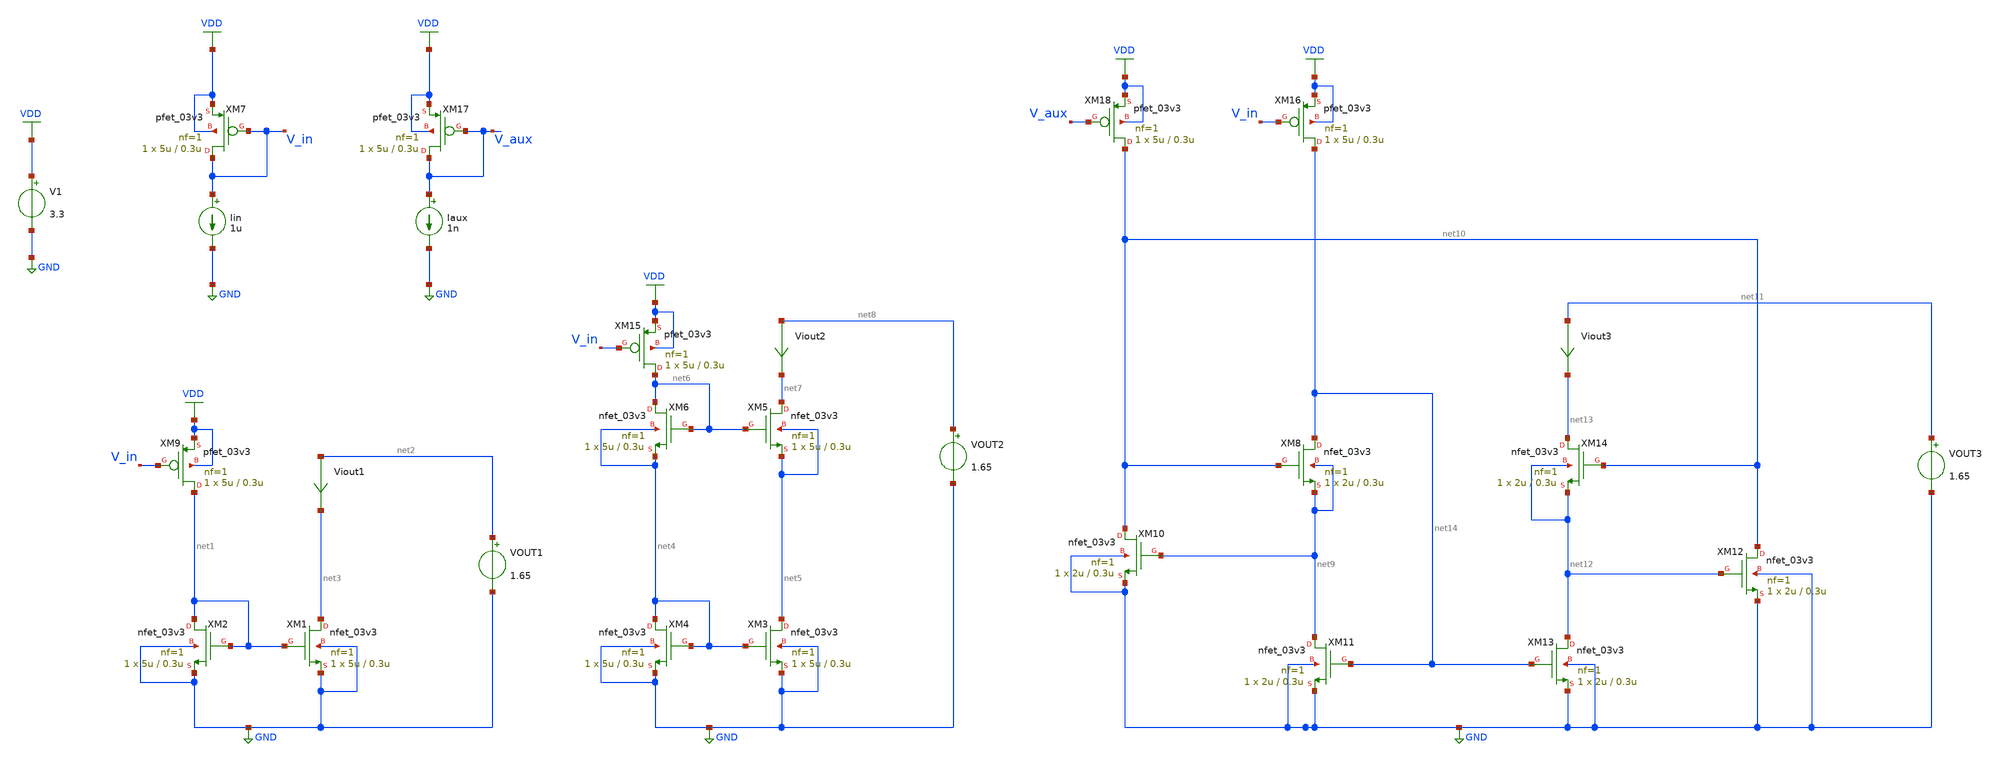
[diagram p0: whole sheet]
** sch_path: blocks/composite/regulated_cascoded_cmirror/xschem/current_mirror.sch
**.subckt current_mirror
XM1 net3 net1 GND GND nfet_03v3 L=0.3u W=5u nf=1 ad='int((nf+1)/2) * W/nf * 0.18u' as='int((nf+2)/2) * W/nf * 0.18u'
+ pd='2*int((nf+1)/2) * (W/nf + 0.18u)' ps='2*int((nf+2)/2) * (W/nf + 0.18u)' nrd='0.18u / W' nrs='0.18u / W'
+ sa=0 sb=0 sd=0 m=1
XM2 net1 net1 GND GND nfet_03v3 L=0.3u W=5u nf=1 ad='int((nf+1)/2) * W/nf * 0.18u' as='int((nf+2)/2) * W/nf * 0.18u'
+ pd='2*int((nf+1)/2) * (W/nf + 0.18u)' ps='2*int((nf+2)/2) * (W/nf + 0.18u)' nrd='0.18u / W' nrs='0.18u / W'
+ sa=0 sb=0 sd=0 m=1
VOUT1 net2 GND 1.65
.save i(vout1)
Viout1 net2 net3 0
.save i(viout1)
XM3 net5 net4 GND GND nfet_03v3 L=0.3u W=5u nf=1 ad='int((nf+1)/2) * W/nf * 0.18u' as='int((nf+2)/2) * W/nf * 0.18u'
+ pd='2*int((nf+1)/2) * (W/nf + 0.18u)' ps='2*int((nf+2)/2) * (W/nf + 0.18u)' nrd='0.18u / W' nrs='0.18u / W'
+ sa=0 sb=0 sd=0 m=1
XM4 net4 net4 GND GND nfet_03v3 L=0.3u W=5u nf=1 ad='int((nf+1)/2) * W/nf * 0.18u' as='int((nf+2)/2) * W/nf * 0.18u'
+ pd='2*int((nf+1)/2) * (W/nf + 0.18u)' ps='2*int((nf+2)/2) * (W/nf + 0.18u)' nrd='0.18u / W' nrs='0.18u / W'
+ sa=0 sb=0 sd=0 m=1
VOUT2 net8 GND 1.65
.save i(vout2)
Viout2 net8 net7 0
.save i(viout2)
XM5 net7 net6 net5 net5 nfet_03v3 L=0.3u W=5u nf=1 ad='int((nf+1)/2) * W/nf * 0.18u' as='int((nf+2)/2) * W/nf * 0.18u'
+ pd='2*int((nf+1)/2) * (W/nf + 0.18u)' ps='2*int((nf+2)/2) * (W/nf + 0.18u)' nrd='0.18u / W' nrs='0.18u / W'
+ sa=0 sb=0 sd=0 m=1
XM6 net6 net6 net4 net4 nfet_03v3 L=0.3u W=5u nf=1 ad='int((nf+1)/2) * W/nf * 0.18u' as='int((nf+2)/2) * W/nf * 0.18u'
+ pd='2*int((nf+1)/2) * (W/nf + 0.18u)' ps='2*int((nf+2)/2) * (W/nf + 0.18u)' nrd='0.18u / W' nrs='0.18u / W'
+ sa=0 sb=0 sd=0 m=1
VOUT3 net11 GND 1.65
.save i(vout3)
Viout3 net11 net13 0
.save i(viout3)
XM10 net10 net9 GND GND nfet_03v3 L=0.3u W=2u nf=1 ad='int((nf+1)/2) * W/nf * 0.18u' as='int((nf+2)/2) * W/nf * 0.18u'
+ pd='2*int((nf+1)/2) * (W/nf + 0.18u)' ps='2*int((nf+2)/2) * (W/nf + 0.18u)' nrd='0.18u / W' nrs='0.18u / W'
+ sa=0 sb=0 sd=0 m=1
XM8 net14 net10 net9 net9 nfet_03v3 L=0.3u W=2u nf=1 ad='int((nf+1)/2) * W/nf * 0.18u' as='int((nf+2)/2) * W/nf * 0.18u'
+ pd='2*int((nf+1)/2) * (W/nf + 0.18u)' ps='2*int((nf+2)/2) * (W/nf + 0.18u)' nrd='0.18u / W' nrs='0.18u / W'
+ sa=0 sb=0 sd=0 m=1
XM11 net9 net14 GND GND nfet_03v3 L=0.3u W=2u nf=1 ad='int((nf+1)/2) * W/nf * 0.18u' as='int((nf+2)/2) * W/nf * 0.18u'
+ pd='2*int((nf+1)/2) * (W/nf + 0.18u)' ps='2*int((nf+2)/2) * (W/nf + 0.18u)' nrd='0.18u / W' nrs='0.18u / W'
+ sa=0 sb=0 sd=0 m=1
XM12 net10 net12 GND GND nfet_03v3 L=0.3u W=2u nf=1 ad='int((nf+1)/2) * W/nf * 0.18u' as='int((nf+2)/2) * W/nf * 0.18u'
+ pd='2*int((nf+1)/2) * (W/nf + 0.18u)' ps='2*int((nf+2)/2) * (W/nf + 0.18u)' nrd='0.18u / W' nrs='0.18u / W'
+ sa=0 sb=0 sd=0 m=1
XM13 net12 net14 GND GND nfet_03v3 L=0.3u W=2u nf=1 ad='int((nf+1)/2) * W/nf * 0.18u' as='int((nf+2)/2) * W/nf * 0.18u'
+ pd='2*int((nf+1)/2) * (W/nf + 0.18u)' ps='2*int((nf+2)/2) * (W/nf + 0.18u)' nrd='0.18u / W' nrs='0.18u / W'
+ sa=0 sb=0 sd=0 m=1
XM14 net13 net10 net12 net12 nfet_03v3 L=0.3u W=2u nf=1 ad='int((nf+1)/2) * W/nf * 0.18u' as='int((nf+2)/2) * W/nf * 0.18u'
+ pd='2*int((nf+1)/2) * (W/nf + 0.18u)' ps='2*int((nf+2)/2) * (W/nf + 0.18u)' nrd='0.18u / W' nrs='0.18u / W'
+ sa=0 sb=0 sd=0 m=1
V1 VDD GND 3.3
XM7 V_in V_in VDD VDD pfet_03v3 L=0.3u W=5u nf=1 ad='int((nf+1)/2) * W/nf * 0.18u' as='int((nf+2)/2) * W/nf * 0.18u'
+ pd='2*int((nf+1)/2) * (W/nf + 0.18u)' ps='2*int((nf+2)/2) * (W/nf + 0.18u)' nrd='0.18u / W' nrs='0.18u / W'
+ sa=0 sb=0 sd=0 m=1
Iin V_in GND 1u
XM9 net1 V_in VDD VDD pfet_03v3 L=0.3u W=5u nf=1 ad='int((nf+1)/2) * W/nf * 0.18u' as='int((nf+2)/2) * W/nf * 0.18u'
+ pd='2*int((nf+1)/2) * (W/nf + 0.18u)' ps='2*int((nf+2)/2) * (W/nf + 0.18u)' nrd='0.18u / W' nrs='0.18u / W'
+ sa=0 sb=0 sd=0 m=1
XM15 net6 V_in VDD VDD pfet_03v3 L=0.3u W=5u nf=1 ad='int((nf+1)/2) * W/nf * 0.18u' as='int((nf+2)/2) * W/nf * 0.18u'
+ pd='2*int((nf+1)/2) * (W/nf + 0.18u)' ps='2*int((nf+2)/2) * (W/nf + 0.18u)' nrd='0.18u / W' nrs='0.18u / W'
+ sa=0 sb=0 sd=0 m=1
XM16 net14 V_in VDD VDD pfet_03v3 L=0.3u W=5u nf=1 ad='int((nf+1)/2) * W/nf * 0.18u' as='int((nf+2)/2) * W/nf * 0.18u'
+ pd='2*int((nf+1)/2) * (W/nf + 0.18u)' ps='2*int((nf+2)/2) * (W/nf + 0.18u)' nrd='0.18u / W' nrs='0.18u / W'
+ sa=0 sb=0 sd=0 m=1
XM17 V_aux V_aux VDD VDD pfet_03v3 L=0.3u W=5u nf=1 ad='int((nf+1)/2) * W/nf * 0.18u' as='int((nf+2)/2) * W/nf * 0.18u'
+ pd='2*int((nf+1)/2) * (W/nf + 0.18u)' ps='2*int((nf+2)/2) * (W/nf + 0.18u)' nrd='0.18u / W' nrs='0.18u / W'
+ sa=0 sb=0 sd=0 m=1
Iaux V_aux GND 1n
XM18 net10 V_aux VDD VDD pfet_03v3 L=0.3u W=5u nf=1 ad='int((nf+1)/2) * W/nf * 0.18u' as='int((nf+2)/2) * W/nf * 0.18u'
+ pd='2*int((nf+1)/2) * (W/nf + 0.18u)' ps='2*int((nf+2)/2) * (W/nf + 0.18u)' nrd='0.18u / W' nrs='0.18u / W'
+ sa=0 sb=0 sd=0 m=1
**** begin user architecture code



.option savecurrent
.control
save all

** Plot Vanilla Current Mirror
dc VOUT1 0 3.3 0.01

setplot dc1
let i_vanilla = viout1#branch
plot i_vanilla

dc VOUT2 0 3.3 0.01
setplot dc2
let i_biased = viout2#branch
plot i_biased

dc VOUT3 0 3.3 0.01 Iaux 50p 1n 100p
setplot dc3
let i_cascoded = viout3#branch
plot i_cascoded

write current_mirror.raw viout1#branch viout2#branch viout3#branch
.endc



.include /foss/pdks/gf180mcuD/libs.tech/ngspice/design.ngspice
.lib /foss/pdks/gf180mcuD/libs.tech/ngspice/sm141064.ngspice typical


**** end user architecture code
**.ends
.GLOBAL GND
.GLOBAL VDD
.end
